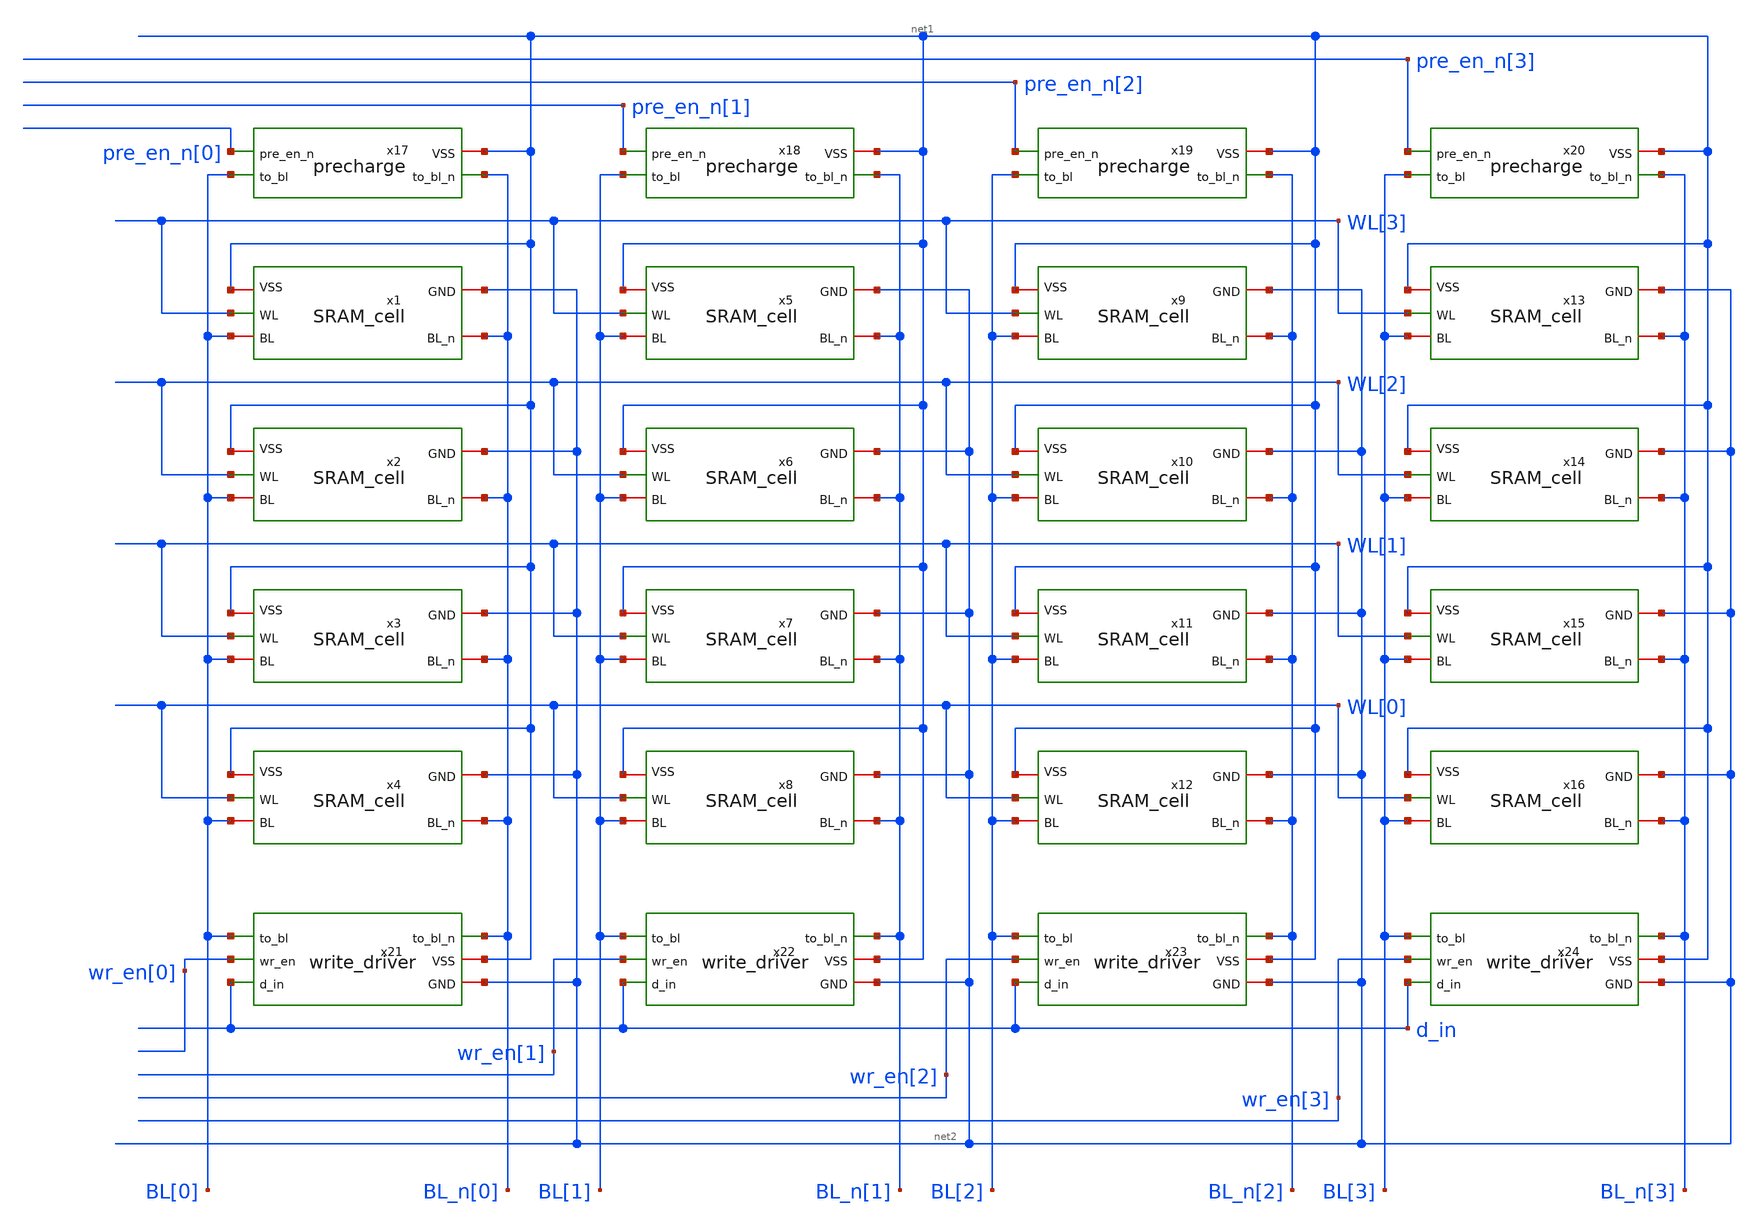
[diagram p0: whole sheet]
** sch_path: 4x4_SRAM.sch
**.subckt 4x4_SRAM
x1 WL[3] net1 BL_n[0] BL[0] net2 SRAM_cell
x2 WL[2] net1 BL_n[0] BL[0] net2 SRAM_cell
x3 WL[1] net1 BL_n[0] BL[0] net2 SRAM_cell
x4 WL[0] net1 BL_n[0] BL[0] net2 SRAM_cell
x5 WL[3] net1 BL_n[1] BL[1] net2 SRAM_cell
x6 WL[2] net1 BL_n[1] BL[1] net2 SRAM_cell
x7 WL[1] net1 BL_n[1] BL[1] net2 SRAM_cell
x8 WL[0] net1 BL_n[1] BL[1] net2 SRAM_cell
x9 WL[3] net1 BL_n[2] BL[2] net2 SRAM_cell
x10 WL[2] net1 BL_n[2] BL[2] net2 SRAM_cell
x11 WL[1] net1 BL_n[2] BL[2] net2 SRAM_cell
x12 WL[0] net1 BL_n[2] BL[2] net2 SRAM_cell
x13 WL[3] net1 BL_n[3] BL[3] net2 SRAM_cell
x14 WL[2] net1 BL_n[3] BL[3] net2 SRAM_cell
x15 WL[1] net1 BL_n[3] BL[3] net2 SRAM_cell
x16 WL[0] net1 BL_n[3] BL[3] net2 SRAM_cell
x17 net1 BL_n[0] BL[0] pre_en_n[0] precharge
x18 net1 BL_n[1] BL[1] pre_en_n[1] precharge
x19 net1 BL_n[2] BL[2] pre_en_n[2] precharge
x20 net1 BL_n[3] BL[3] pre_en_n[3] precharge
x21 BL_n[0] BL[0] wr_en[0] net1 d_in net2 write_driver
x22 BL_n[1] BL[1] wr_en[1] net1 d_in net2 write_driver
x23 BL_n[2] BL[2] wr_en[2] net1 d_in net2 write_driver
x24 BL_n[3] BL[3] wr_en[3] net1 d_in net2 write_driver
**.ends

* expanding   symbol:  /home/ee431/workspace/proj_4x4SRAM/SRAM_cell.sym # of pins=5
** sym_path: SRAM_cell.sym
** sch_path: SRAM_cell.sch
.subckt SRAM_cell WL VSS BL_n BL GND
*.ipin WL
*.iopin BL
*.iopin BL_n
*.iopin VSS
*.iopin GND
XM1 Q_n Q GND GND sky130_fd_pr__nfet_01v8 L=0.25 W=1.25 nf=1 ad='int((nf+1)/2) * W/nf * 0.29' as='int((nf+2)/2) * W/nf * 0.29'
+ pd='2*int((nf+1)/2) * (W/nf + 0.29)' ps='2*int((nf+2)/2) * (W/nf + 0.29)' nrd='0.29 / W' nrs='0.29 / W'
+ sa=0 sb=0 sd=0 mult=1 m=1
XM2 Q_n Q VSS VSS sky130_fd_pr__pfet_01v8 L=0.25 W=0.5 nf=1 ad='int((nf+1)/2) * W/nf * 0.29' as='int((nf+2)/2) * W/nf * 0.29'
+ pd='2*int((nf+1)/2) * (W/nf + 0.29)' ps='2*int((nf+2)/2) * (W/nf + 0.29)' nrd='0.29 / W' nrs='0.29 / W'
+ sa=0 sb=0 sd=0 mult=1 m=1
XM3 Q Q_n GND GND sky130_fd_pr__nfet_01v8 L=0.25 W=1.25 nf=1 ad='int((nf+1)/2) * W/nf * 0.29' as='int((nf+2)/2) * W/nf * 0.29'
+ pd='2*int((nf+1)/2) * (W/nf + 0.29)' ps='2*int((nf+2)/2) * (W/nf + 0.29)' nrd='0.29 / W' nrs='0.29 / W'
+ sa=0 sb=0 sd=0 mult=1 m=1
XM4 Q Q_n VSS VSS sky130_fd_pr__pfet_01v8 L=0.25 W=0.5 nf=1 ad='int((nf+1)/2) * W/nf * 0.29' as='int((nf+2)/2) * W/nf * 0.29'
+ pd='2*int((nf+1)/2) * (W/nf + 0.29)' ps='2*int((nf+2)/2) * (W/nf + 0.29)' nrd='0.29 / W' nrs='0.29 / W'
+ sa=0 sb=0 sd=0 mult=1 m=1
XM5 Q WL BL GND sky130_fd_pr__nfet_01v8 L=0.25 W=0.75 nf=1 ad='int((nf+1)/2) * W/nf * 0.29' as='int((nf+2)/2) * W/nf * 0.29'
+ pd='2*int((nf+1)/2) * (W/nf + 0.29)' ps='2*int((nf+2)/2) * (W/nf + 0.29)' nrd='0.29 / W' nrs='0.29 / W'
+ sa=0 sb=0 sd=0 mult=1 m=1
XM6 Q_n WL BL_n GND sky130_fd_pr__nfet_01v8 L=0.25 W=0.75 nf=1 ad='int((nf+1)/2) * W/nf * 0.29' as='int((nf+2)/2) * W/nf * 0.29'
+ pd='2*int((nf+1)/2) * (W/nf + 0.29)' ps='2*int((nf+2)/2) * (W/nf + 0.29)' nrd='0.29 / W' nrs='0.29 / W'
+ sa=0 sb=0 sd=0 mult=1 m=1
.ends


* expanding   symbol:  /home/ee431/workspace/proj_4x4SRAM/precharge.sym # of pins=4
** sym_path: precharge.sym
** sch_path: precharge.sch
.subckt precharge VSS to_bl_n to_bl pre_en_n
*.ipin pre_en_n
*.opin to_bl
*.opin to_bl_n
*.iopin VSS
XM1 to_bl_n pre_en_n VSS VSS sky130_fd_pr__pfet_01v8 L=0.25 W=0.5 nf=1 ad='int((nf+1)/2) * W/nf * 0.29'
+ as='int((nf+2)/2) * W/nf * 0.29' pd='2*int((nf+1)/2) * (W/nf + 0.29)' ps='2*int((nf+2)/2) * (W/nf + 0.29)'
+ nrd='0.29 / W' nrs='0.29 / W' sa=0 sb=0 sd=0 mult=1 m=1
XM2 to_bl pre_en_n VSS VSS sky130_fd_pr__pfet_01v8 L=0.25 W=0.5 nf=1 ad='int((nf+1)/2) * W/nf * 0.29'
+ as='int((nf+2)/2) * W/nf * 0.29' pd='2*int((nf+1)/2) * (W/nf + 0.29)' ps='2*int((nf+2)/2) * (W/nf + 0.29)'
+ nrd='0.29 / W' nrs='0.29 / W' sa=0 sb=0 sd=0 mult=1 m=1
.ends


* expanding   symbol:  /home/ee431/workspace/proj_4x4SRAM/write_driver.sym # of pins=6
** sym_path: write_driver.sym
** sch_path: write_driver.sch
.subckt write_driver to_bl_n to_bl wr_en VSS d_in GND
*.ipin d_in
*.ipin wr_en
*.opin to_bl
*.opin to_bl_n
*.iopin VSS
*.iopin GND
XM1 to_bl wr_en d_in GND sky130_fd_pr__nfet_01v8 L=0.25 W=1 nf=1 ad='int((nf+1)/2) * W/nf * 0.29' as='int((nf+2)/2) * W/nf * 0.29'
+ pd='2*int((nf+1)/2) * (W/nf + 0.29)' ps='2*int((nf+2)/2) * (W/nf + 0.29)' nrd='0.29 / W' nrs='0.29 / W'
+ sa=0 sb=0 sd=0 mult=1 m=1
XM2 to_bl_n wr_en d_n GND sky130_fd_pr__nfet_01v8 L=0.25 W=1 nf=1 ad='int((nf+1)/2) * W/nf * 0.29' as='int((nf+2)/2) * W/nf * 0.29'
+ pd='2*int((nf+1)/2) * (W/nf + 0.29)' ps='2*int((nf+2)/2) * (W/nf + 0.29)' nrd='0.29 / W' nrs='0.29 / W'
+ sa=0 sb=0 sd=0 mult=1 m=1
XM3 d_n d_in VSS VSS sky130_fd_pr__pfet_01v8 L=0.25 W=1 nf=1 ad='int((nf+1)/2) * W/nf * 0.29' as='int((nf+2)/2) * W/nf * 0.29'
+ pd='2*int((nf+1)/2) * (W/nf + 0.29)' ps='2*int((nf+2)/2) * (W/nf + 0.29)' nrd='0.29 / W' nrs='0.29 / W'
+ sa=0 sb=0 sd=0 mult=1 m=1
XM4 d_n d_in GND GND sky130_fd_pr__nfet_01v8 L=0.25 W=0.5 nf=1 ad='int((nf+1)/2) * W/nf * 0.29' as='int((nf+2)/2) * W/nf * 0.29'
+ pd='2*int((nf+1)/2) * (W/nf + 0.29)' ps='2*int((nf+2)/2) * (W/nf + 0.29)' nrd='0.29 / W' nrs='0.29 / W'
+ sa=0 sb=0 sd=0 mult=1 m=1
.ends

.end
